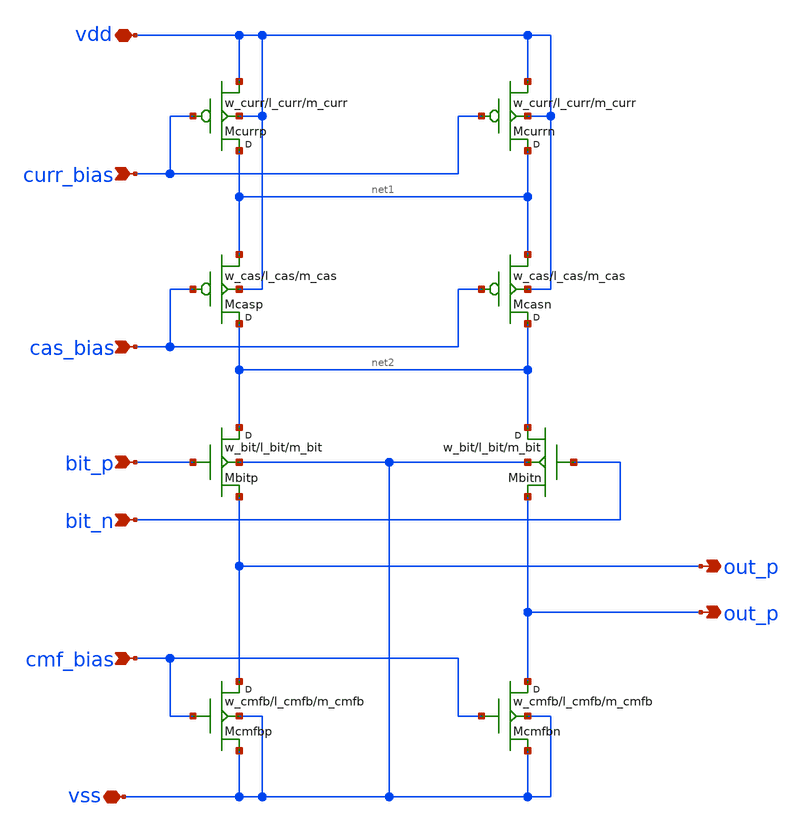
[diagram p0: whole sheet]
** sch_path: design/dac_unit_cell/dac_unit_cell.sch
**.subckt dac_unit_cell vdd vss curr_bias bit_p bit_n cmf_bias out_p out_p cas_bias
*.iopin vdd
*.iopin vss
*.ipin curr_bias
*.ipin bit_p
*.ipin bit_n
*.ipin cmf_bias
*.opin out_p
*.opin out_p
*.ipin cas_bias
Mcmfbp out_p cmf_bias vss vss nmos w=w_cmfb l=l_cmfb m=m_cmfb
Mbitp net2 bit_p out_p vss nmos w=w_bit l=l_bit m=m_bit
Mbitn net2 bit_n out_p vss nmos w=w_bit l=l_bit m=m_bit
Mcmfbn out_p cmf_bias vss vss nmos w=w_cmfb l=l_cmfb m=m_cmfb
Mcurrn net1 curr_bias vdd vdd pmos w=w_curr l=l_curr m=m_curr
Mcurrp net1 curr_bias vdd vdd pmos w=w_curr l=l_curr m=m_curr
Mcasn net2 cas_bias net1 vdd pmos w=w_cas l=l_cas m=m_cas
Mcasp net2 cas_bias net1 vdd pmos w=w_cas l=l_cas m=m_cas
**.ends
.end
